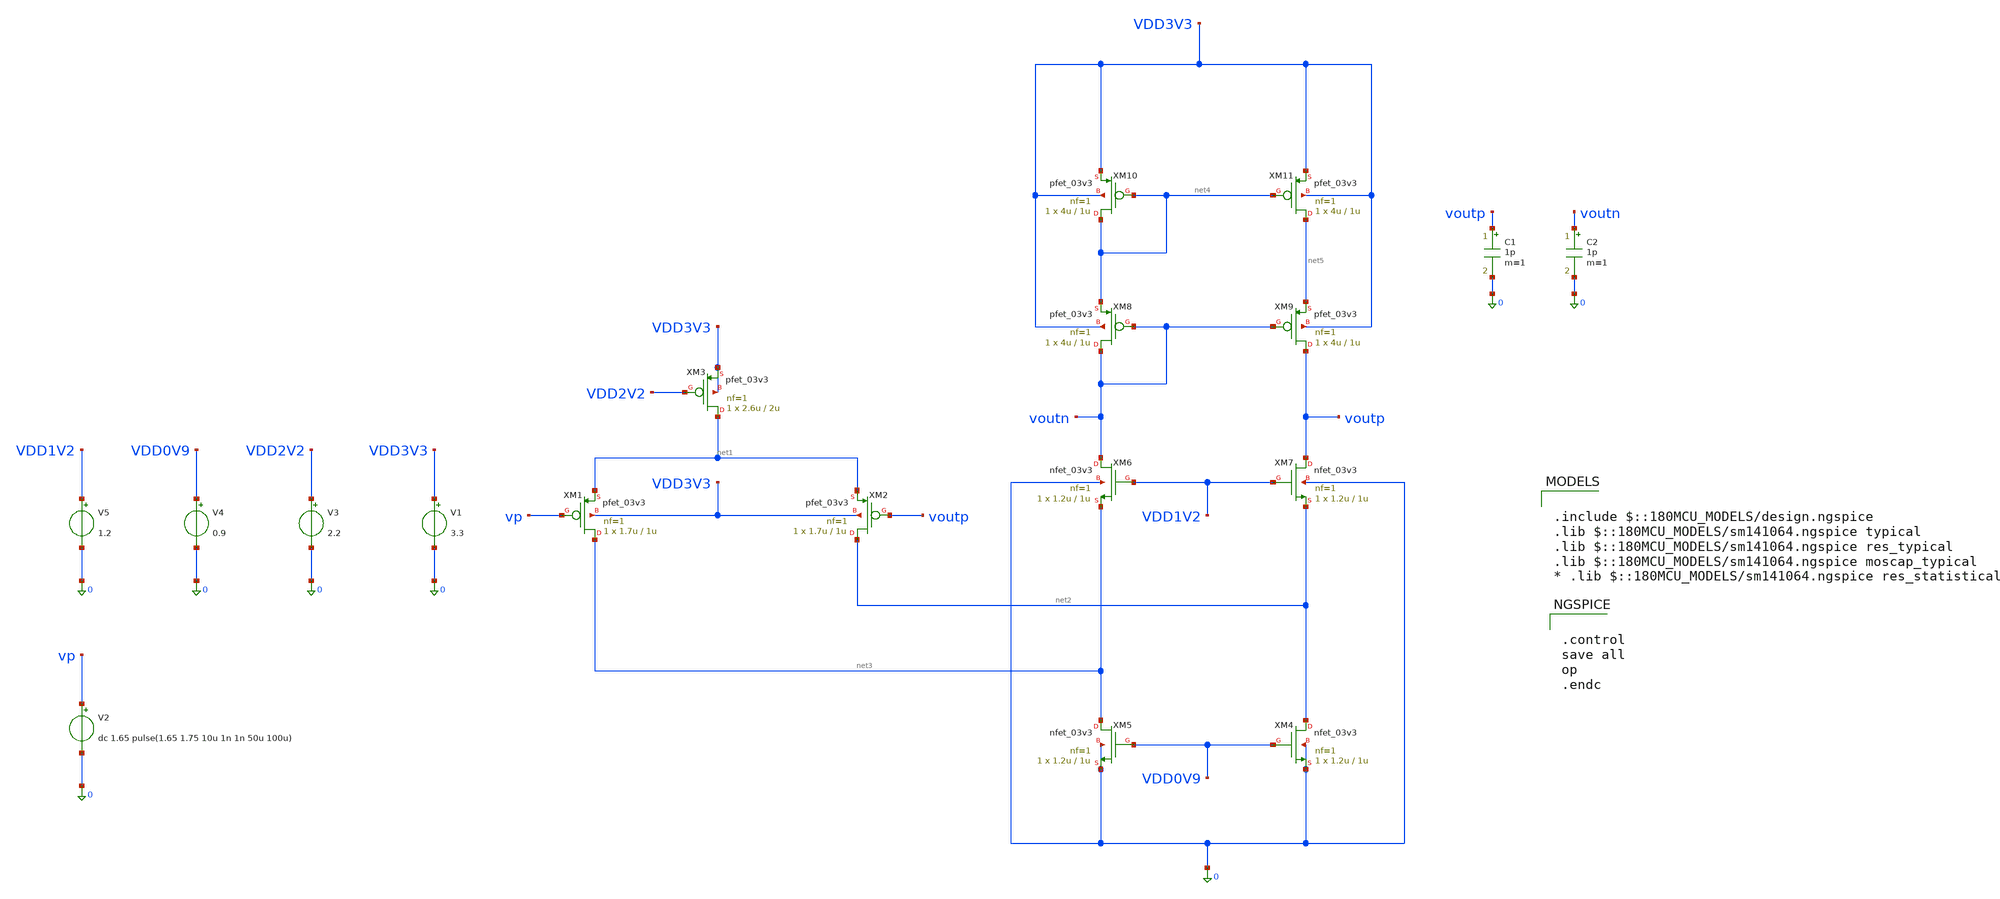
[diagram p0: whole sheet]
** sch_path: designs/AutoECG/folded_cascode/tb_folded_cascode_v1.sch
**.subckt tb_folded_cascode_v1
XM1 net3 vp net1 VDD3V3 pfet_03v3 L=1u W=1.7u nf=1 ad='int((nf+1)/2) * W/nf * 0.18u' as='int((nf+2)/2) * W/nf * 0.18u'
+ pd='2*int((nf+1)/2) * (W/nf + 0.18u)' ps='2*int((nf+2)/2) * (W/nf + 0.18u)' nrd='0.18u / W' nrs='0.18u / W'
+ sa=0 sb=0 sd=0 m=1
V1 VDD3V3 0 3.3
XM2 net2 voutp net1 VDD3V3 pfet_03v3 L=1u W=1.7u nf=1 ad='int((nf+1)/2) * W/nf * 0.18u' as='int((nf+2)/2) * W/nf * 0.18u'
+ pd='2*int((nf+1)/2) * (W/nf + 0.18u)' ps='2*int((nf+2)/2) * (W/nf + 0.18u)' nrd='0.18u / W' nrs='0.18u / W'
+ sa=0 sb=0 sd=0 m=1
V2 vp 0 dc 1.65 pulse(1.65 1.75 10u 1n 1n 50u 100u)
XM3 net1 VDD2V2 VDD3V3 VDD3V3 pfet_03v3 L=2u W=2.6u nf=1 ad='int((nf+1)/2) * W/nf * 0.18u' as='int((nf+2)/2) * W/nf * 0.18u'
+ pd='2*int((nf+1)/2) * (W/nf + 0.18u)' ps='2*int((nf+2)/2) * (W/nf + 0.18u)' nrd='0.18u / W' nrs='0.18u / W'
+ sa=0 sb=0 sd=0 m=1
V3 VDD2V2 0 2.2
XM5 net3 VDD0V9 0 0 nfet_03v3 L=1u W=1.2u nf=1 ad='int((nf+1)/2) * W/nf * 0.18u' as='int((nf+2)/2) * W/nf * 0.18u'
+ pd='2*int((nf+1)/2) * (W/nf + 0.18u)' ps='2*int((nf+2)/2) * (W/nf + 0.18u)' nrd='0.18u / W' nrs='0.18u / W'
+ sa=0 sb=0 sd=0 m=1
V4 VDD0V9 0 0.9
XM4 net2 VDD0V9 0 0 nfet_03v3 L=1u W=1.2u nf=1 ad='int((nf+1)/2) * W/nf * 0.18u' as='int((nf+2)/2) * W/nf * 0.18u'
+ pd='2*int((nf+1)/2) * (W/nf + 0.18u)' ps='2*int((nf+2)/2) * (W/nf + 0.18u)' nrd='0.18u / W' nrs='0.18u / W'
+ sa=0 sb=0 sd=0 m=1
XM6 voutn VDD1V2 net3 0 nfet_03v3 L=1u W=1.2u nf=1 ad='int((nf+1)/2) * W/nf * 0.18u' as='int((nf+2)/2) * W/nf * 0.18u'
+ pd='2*int((nf+1)/2) * (W/nf + 0.18u)' ps='2*int((nf+2)/2) * (W/nf + 0.18u)' nrd='0.18u / W' nrs='0.18u / W'
+ sa=0 sb=0 sd=0 m=1
XM7 voutp VDD1V2 net2 0 nfet_03v3 L=1u W=1.2u nf=1 ad='int((nf+1)/2) * W/nf * 0.18u' as='int((nf+2)/2) * W/nf * 0.18u'
+ pd='2*int((nf+1)/2) * (W/nf + 0.18u)' ps='2*int((nf+2)/2) * (W/nf + 0.18u)' nrd='0.18u / W' nrs='0.18u / W'
+ sa=0 sb=0 sd=0 m=1
V5 VDD1V2 0 1.2
XM10 net4 net4 VDD3V3 VDD3V3 pfet_03v3 L=1u W=4u nf=1 ad='int((nf+1)/2) * W/nf * 0.18u' as='int((nf+2)/2) * W/nf * 0.18u'
+ pd='2*int((nf+1)/2) * (W/nf + 0.18u)' ps='2*int((nf+2)/2) * (W/nf + 0.18u)' nrd='0.18u / W' nrs='0.18u / W'
+ sa=0 sb=0 sd=0 m=1
XM11 net5 net4 VDD3V3 VDD3V3 pfet_03v3 L=1u W=4u nf=1 ad='int((nf+1)/2) * W/nf * 0.18u' as='int((nf+2)/2) * W/nf * 0.18u'
+ pd='2*int((nf+1)/2) * (W/nf + 0.18u)' ps='2*int((nf+2)/2) * (W/nf + 0.18u)' nrd='0.18u / W' nrs='0.18u / W'
+ sa=0 sb=0 sd=0 m=1
XM8 voutn voutn net4 VDD3V3 pfet_03v3 L=1u W=4u nf=1 ad='int((nf+1)/2) * W/nf * 0.18u' as='int((nf+2)/2) * W/nf * 0.18u'
+ pd='2*int((nf+1)/2) * (W/nf + 0.18u)' ps='2*int((nf+2)/2) * (W/nf + 0.18u)' nrd='0.18u / W' nrs='0.18u / W'
+ sa=0 sb=0 sd=0 m=1
XM9 voutp voutn net5 VDD3V3 pfet_03v3 L=1u W=4u nf=1 ad='int((nf+1)/2) * W/nf * 0.18u' as='int((nf+2)/2) * W/nf * 0.18u'
+ pd='2*int((nf+1)/2) * (W/nf + 0.18u)' ps='2*int((nf+2)/2) * (W/nf + 0.18u)' nrd='0.18u / W' nrs='0.18u / W'
+ sa=0 sb=0 sd=0 m=1
C1 voutp 0 1p m=1
C2 voutn 0 1p m=1
**** begin user architecture code

.include $::180MCU_MODELS/design.ngspice
.lib $::180MCU_MODELS/sm141064.ngspice typical
.lib $::180MCU_MODELS/sm141064.ngspice res_typical
.lib $::180MCU_MODELS/sm141064.ngspice moscap_typical
* .lib $::180MCU_MODELS/sm141064.ngspice res_statistical



.control
save all
op
.endc




.control
  * 1. Corremos la simulación AC extendida hasta 100 GHz (100g)
  ac dec 20 1 100g

  * Definición de tu salida (resta de nodos):
  let vout = v(voutp) - v(voutn)

  * NUEVO PASO: Creamos un vector nativo de magnitud para que 'meas' no falle
  let vout_magnitude = mag(vout)

  * 2. Calculamos la ganancia DC usando directamente el vector de salida v(vout)
  * Usamos [0] para extraer el primer punto (1 Hz)
  let dc_gain_linear = vout_magnitude[0]
  let dc_gain_db = 20 * log10(dc_gain_linear)
  print dc_gain_db

  * ==========================================
  * COMANDOS DE MEDICIÓN CORREGIDOS Y BLINDADOS:
  * ==========================================

  * A. Buscamos la frecuencia de corte a -3 dB
  let target_3db = dc_gain_linear * 0.707
  meas ac f_corte when vout_magnitude=target_3db

  * B. Buscamos el GBW (Magnitud = 1)
  meas ac gbw_freq when vout_magnitude=1

  * ==========================================

  * 3. Gráfica original
  plot mag(vout)
.endc




* --- 1. PARÁMETROS GLOBALES ANTICRISIS (SKYWATER) ---
.param sw_stat_mismatch=0
.param mis_vth=0
.param mis_k=0

* --- 2. BLOQUE DE CONTROL PARA TRANSITORIO Y GRÁFICA ---
.control
  * Limpiamos residuos de simulaciones previas
  clearsub

  * Corremos la simulación temporal por 120 microsegundos
  * Con pasos de 10 nanosegundos para ver los detalles con resolución limpia
  tran 10n 120u

  * 3. Graficamos directamente el nodo que me pediste
  * También agregamos v(vinp) para que puedas comparar visualmente la entrada vs la salida
  plot v(voutp) v(vp)
  meas tran v_min min v(voutp)
  meas tran v_max max v(voutp)

  let v_amp = v_max - v_min
  let v_10 = v_min + (0.1 * v_amp)
  let v_80 = v_min + (0.8 * v_amp)

  meas tran tr1 when v(voutp)={$&v_10} rise=1
  meas tran tr2 when v(voutp)={$&v_80} rise=1
  let sr_rise = (v_80 - v_10) / (tr2 - tr1)

  meas tran tf1 when v(voutp)={$&v_80} fall=1
  meas tran tf2 when v(voutp)={$&v_10} fall=1
  let sr_fall = (v_80 - v_10) / (tf2 - tf1)

  print sr_rise
  print sr_fall


.endc


**** end user architecture code
**.ends
.end
